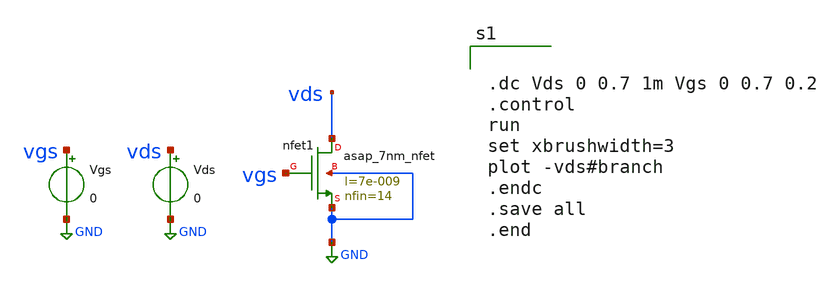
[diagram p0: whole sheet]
** sch_path: Xschem_ASAP7/nfet.sch
**.subckt nfet
Xnfet1 vds vgs GND GND asap_7nm_nfet l=7e-009 nfin=14
Vgs vgs GND 0
Vds vds GND 0
**** begin user architecture code


.dc Vds 0 0.7 1m Vgs 0 0.7 0.2
.control
run
set xbrushwidth=3
plot -vds#branch
.endc
.save all
.end


**** end user architecture code
**.ends
.GLOBAL GND
.end
